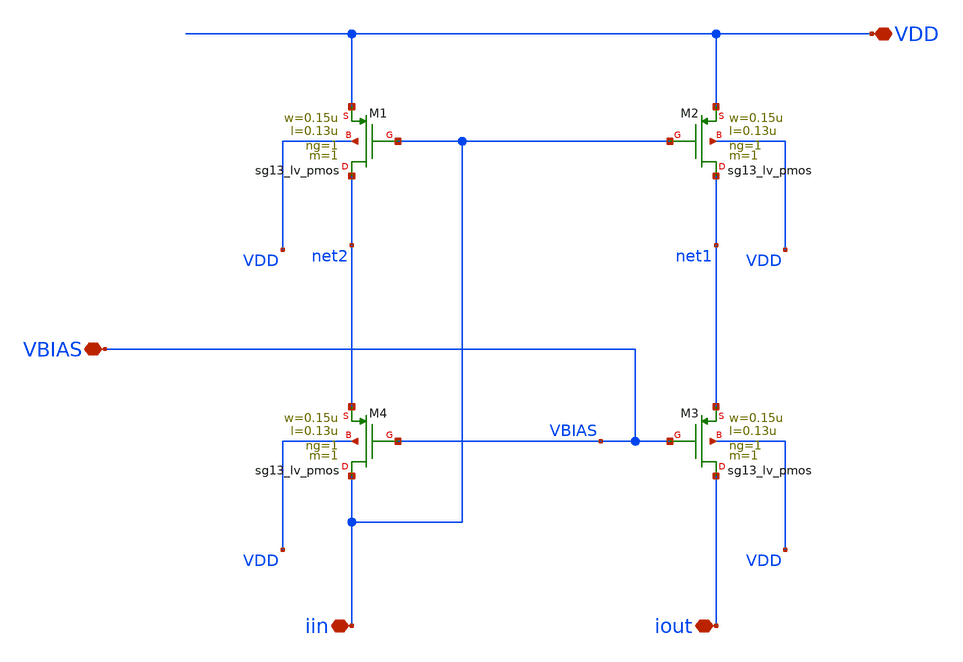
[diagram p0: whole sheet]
** sch_path: analog-db/templates/current_mirror/pmos_current_source/low_voltage_cascode_current_mirror.sch
* Copyright 2026 MacAnalog Research Group
**.subckt low_voltage_cascode_current_mirror VDD iin VBIAS iout
*.iopin VDD
*.iopin iin
*.iopin VBIAS
*.iopin iout
XM1 net2 iin VDD VDD sg13_lv_pmos w=0.15u l=0.13u ng=1 m=1 mm_ok=1
XM2 net1 iin VDD VDD sg13_lv_pmos w=0.15u l=0.13u ng=1 m=1 mm_ok=1
XM3 iout VBIAS net1 VDD sg13_lv_pmos w=0.15u l=0.13u ng=1 m=1 mm_ok=1
XM4 iin VBIAS net2 VDD sg13_lv_pmos w=0.15u l=0.13u ng=1 m=1 mm_ok=1
**.ends
.end
